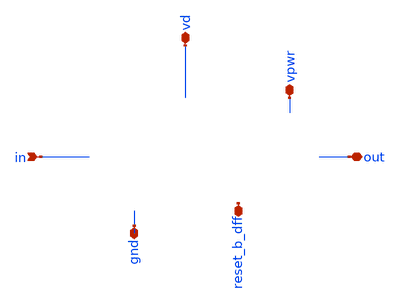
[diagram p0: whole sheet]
** sch_path: sigma-delta_modulator/xschem/sigma-delta-pex.sch
* Copyright 2020 Stefan Frederik Schippers
* Licensed under the Apache License, Version 2.0 (the "License");
* you may not use this file except in compliance with the License.
* You may obtain a copy of the License at
* https://www.apache.org/licenses/LICENSE-2.0
* Unless required by applicable law or agreed to in writing, software
* distributed under the License is distributed on an "AS IS" BASIS,
* WITHOUT WARRANTIES OR CONDITIONS OF ANY KIND, either express or implied.
* See the License for the specific language governing permissions and
* limitations under the License.
**.subckt sigma-delta-pex in gnd out reset_b_dff vpwr vd
*.ipin in
*.iopin gnd
*.iopin out
*.iopin reset_b_dff
*.iopin vpwr
*.iopin vd
**** begin user architecture code



* NGSPICE file created from sigma-delta.ext - technology: sky130A

*.subckt sigma-delta in gnd reset_b_dff vd clk vpwr out
X0 a_n2266_4800# a_n2100_3468# gnd.t0 sky130_fd_pr__res_xhigh_po_0p35 l=4.5
X1 a_n1124_4800# a_n958_3468# gnd.t40 sky130_fd_pr__res_xhigh_po_0p35 l=4.5
X2 vpwr.t5 a_n1599_1969# a_n1612_2361# vpwr.t4 sky130_fd_pr__pfet_01v8_hvt ad=0.0819 pd=0.81
+ as=0.0567 ps=0.69 w=0.42 l=0.15
X3 a_n1599_1969# a_n1774_1995# a_n1420_1995# gnd.t39 sky130_fd_pr__nfet_01v8 ad=0.109 pd=1.36
+ as=0.064 ps=0.725 w=0.42 l=0.15
X4 a_n2231_2361# reset_b_dff.t0 vpwr.t19 vpwr.t18 sky130_fd_pr__pfet_01v8_hvt ad=0.109 pd=1.36
+ as=0.0703 ps=0.755 w=0.42 l=0.15
X5 a_n1599_1969# reset_b_dff.t1 vpwr.t7 vpwr.t6 sky130_fd_pr__pfet_01v8_hvt ad=0.0567 pd=0.69
+ as=0.0819 ps=0.81 w=0.42 l=0.15
X6 x1.Q a_n1599_1969# vpwr.t3 vpwr.t2 sky130_fd_pr__pfet_01v8_hvt ad=0.28 pd=2.56 as=0.213 ps=1.67
+ w=1 l=0.15
X7 out.t0 a_n1035_1995# gnd.t23 gnd.t22 sky130_fd_pr__nfet_01v8 ad=0.169 pd=1.82 as=0.1 ps=0.985
+ w=0.65 l=0.15
X8 a_n2243_1995# a_n2689_1995# a_n2339_1995# gnd.t21 sky130_fd_pr__nfet_01v8 ad=0.14 pd=1.1
+ as=0.0594 ps=0.69 w=0.36 l=0.15
X9 a_n1665_1995# a_n2855_1995# a_n1774_1995# gnd.t19 sky130_fd_pr__nfet_01v8 ad=0.0669 pd=0.75
+ as=0.0711 ps=0.755 w=0.36 l=0.15
X10 gnd.t26 a_n1768_3468# x1.D gnd.t25 sky130_fd_pr__nfet_01v8 ad=0.29 pd=2.58 as=0.29 ps=2.58 w=1
+ l=0.15
X11 a_n792_4800# a_n626_3468# gnd.t38 sky130_fd_pr__res_xhigh_po_0p35 l=4.5
X12 a_n2231_2361# a_n2855_1995# a_n2339_1995# vpwr.t13 sky130_fd_pr__pfet_01v8_hvt ad=0.116 pd=0.97
+ as=0.0724 ps=0.765 w=0.42 l=0.15
X13 a_n2689_1995# a_n2855_1995# gnd.t18 gnd.t17 sky130_fd_pr__nfet_01v8 ad=0.109 pd=1.36 as=0.0567
+ ps=0.69 w=0.42 l=0.15
X14 a_n1934_4800# a_n2100_3468# gnd.t29 sky130_fd_pr__res_xhigh_po_0p35 l=4.5
X15 gnd.t12 reset_b_dff.t2 a_n2077_1995# gnd.t11 sky130_fd_pr__nfet_01v8 ad=0.135 pd=1.15 as=0.0441
+ ps=0.63 w=0.42 l=0.15
X16 a_n2598_4800# a_n2764_3468# gnd.t44 sky130_fd_pr__res_xhigh_po_0p35 l=4.5
X17 gnd.t8 a_n1599_1969# a_n1665_1995# gnd.t7 sky130_fd_pr__nfet_01v8 ad=0.125 pd=1.01 as=0.0669
+ ps=0.75 w=0.42 l=0.15
X18 vd.t1 a_n1768_3468# x1.D vd.t0 sky130_fd_pr__pfet_01v8 ad=0.87 pd=6.58 as=0.87 ps=6.58 w=3
+ l=0.15
X19 a_n1456_4800# a_n1768_3468# gnd.t1 sky130_fd_pr__res_xhigh_po_0p35 l=4.5
X20 vpwr.t1 a_n1599_1969# a_n1035_1995# vpwr.t0 sky130_fd_pr__pfet_01v8_hvt ad=0.154 pd=1.34
+ as=0.166 ps=1.8 w=0.64 l=0.15
X21 a_n1774_1995# a_n2855_1995# a_n2121_2237# vpwr.t12 sky130_fd_pr__pfet_01v8_hvt ad=0.0588 pd=0.7
+ as=0.129 ps=1.18 w=0.42 l=0.15
X22 a_n2077_1995# a_n2121_2237# a_n2243_1995# gnd.t36 sky130_fd_pr__nfet_01v8 ad=0.0441 pd=0.63
+ as=0.14 ps=1.1 w=0.42 l=0.15
X23 a_n2266_4800# a_n2432_3468# gnd.t37 sky130_fd_pr__res_xhigh_po_0p35 l=4.5
X24 a_n1124_4800# a_n1290_3468# gnd.t33 sky130_fd_pr__res_xhigh_po_0p35 l=4.5
X25 a_n2121_2237# a_n2339_1995# vpwr.t9 vpwr.t8 sky130_fd_pr__pfet_01v8_hvt ad=0.129 pd=1.18
+ as=0.218 ps=2.2 w=0.84 l=0.15
X26 a_n460_4800# x1.Q gnd.t13 sky130_fd_pr__res_xhigh_po_0p35 l=4.5
X27 vpwr.t21 clk.t0 a_n2855_1995# vpwr.t20 sky130_fd_pr__pfet_01v8_hvt ad=0.0864 pd=0.91 as=0.166
+ ps=1.8 w=0.64 l=0.15
X28 out.t1 a_n1035_1995# vpwr.t17 vpwr.t16 sky130_fd_pr__pfet_01v8_hvt ad=0.26 pd=2.52 as=0.154
+ ps=1.34 w=1 l=0.15
X29 gnd.t6 a_n1599_1969# a_n1035_1995# gnd.t5 sky130_fd_pr__nfet_01v8 ad=0.1 pd=0.985 as=0.109
+ ps=1.36 w=0.42 l=0.15
X30 vpwr.t23 a_n2121_2237# a_n2231_2361# vpwr.t22 sky130_fd_pr__pfet_01v8_hvt ad=0.0703 pd=0.755
+ as=0.116 ps=0.97 w=0.42 l=0.15
X31 a_n2121_2237# a_n2339_1995# gnd.t15 gnd.t14 sky130_fd_pr__nfet_01v8 ad=0.0999 pd=0.985 as=0.135
+ ps=1.15 w=0.64 l=0.15
X32 a_n1774_1995# a_n2689_1995# a_n2121_2237# gnd.t20 sky130_fd_pr__nfet_01v8 ad=0.0711 pd=0.755
+ as=0.0999 ps=0.985 w=0.36 l=0.15
X33 a_n1612_2361# a_n2689_1995# a_n1774_1995# vpwr.t15 sky130_fd_pr__pfet_01v8_hvt ad=0.0567 pd=0.69
+ as=0.0588 ps=0.7 w=0.42 l=0.15
X34 a_n2339_1995# a_n2855_1995# a_n2434_1995# gnd.t16 sky130_fd_pr__nfet_01v8 ad=0.0594 pd=0.69
+ as=0.066 ps=0.745 w=0.36 l=0.15
X35 a_n2434_1995# x1.D gnd.t42 gnd.t41 sky130_fd_pr__nfet_01v8 ad=0.066 pd=0.745 as=0.221 ps=1.89
+ w=0.42 l=0.15
X36 a_n460_4800# a_n626_3468# gnd.t2 sky130_fd_pr__res_xhigh_po_0p35 l=4.5
X37 a_n2434_1995# x1.D vpwr.t27 vpwr.t26 sky130_fd_pr__pfet_01v8_hvt ad=0.0651 pd=0.73 as=0.109
+ ps=1.36 w=0.42 l=0.15
X38 vpwr.t25 a_n1774_1995# a_n1599_1969# vpwr.t24 sky130_fd_pr__pfet_01v8_hvt ad=0.213 pd=1.67
+ as=0.0567 ps=0.69 w=0.42 l=0.15
X39 a_n2930_4800# a_n2764_3468# gnd.t10 sky130_fd_pr__res_xhigh_po_0p35 l=4.5
X40 gnd.t28 clk.t1 a_n2855_1995# gnd.t27 sky130_fd_pr__nfet_01v8 ad=0.0567 pd=0.69 as=0.109 ps=1.36
+ w=0.42 l=0.15
X41 a_n1768_3468# gnd.t24 sky130_fd_pr__cap_mim_m3_1 l=27.2 w=27.2
X42 a_n1420_1995# reset_b_dff.t3 gnd.t32 gnd.t31 sky130_fd_pr__nfet_01v8 ad=0.064 pd=0.725 as=0.125
+ ps=1.01 w=0.42 l=0.15
X43 a_n1934_4800# a_n1768_3468# gnd.t34 sky130_fd_pr__res_xhigh_po_0p35 l=4.5
X44 a_n792_4800# a_n958_3468# gnd.t35 sky130_fd_pr__res_xhigh_po_0p35 l=4.5
X45 a_n2598_4800# a_n2432_3468# gnd.t9 sky130_fd_pr__res_xhigh_po_0p35 l=4.5
X46 a_n2339_1995# a_n2689_1995# a_n2434_1995# vpwr.t14 sky130_fd_pr__pfet_01v8_hvt ad=0.0724
+ pd=0.765 as=0.0651 ps=0.73 w=0.42 l=0.15
X47 a_n2930_4800# in.t0 gnd.t43 sky130_fd_pr__res_xhigh_po_0p35 l=4.5
X48 a_n1456_4800# a_n1290_3468# gnd.t30 sky130_fd_pr__res_xhigh_po_0p35 l=4.5
X49 a_n2689_1995# a_n2855_1995# vpwr.t11 vpwr.t10 sky130_fd_pr__pfet_01v8_hvt ad=0.166 pd=1.8
+ as=0.0864 ps=0.91 w=0.64 l=0.15
X50 x1.Q a_n1599_1969# gnd.t4 gnd.t3 sky130_fd_pr__nfet_01v8 ad=0.169 pd=1.82 as=0.169 ps=1.82
+ w=0.65 l=0.15
R0 gnd.n65 gnd.t13 3132.98
R1 gnd.t22 gnd.n73 441.774
R2 gnd.t17 gnd.t41 411.14
R3 gnd.t13 gnd.t2 324.911
R4 gnd.t3 gnd.t5 303.115
R5 gnd.t39 gnd.t3 303.115
R6 gnd.n73 gnd.n72 301.113
R7 gnd.t1 gnd.n2 283.973
R8 gnd.t2 gnd.t38 275.286
R9 gnd.t21 gnd.t36 267.644
R10 gnd.t38 gnd.t35 259.007
R11 gnd.t35 gnd.t40 259.007
R12 gnd.t40 gnd.t33 259.007
R13 gnd.t33 gnd.t30 259.007
R14 gnd.t30 gnd.t1 259.007
R15 gnd.t34 gnd.t29 259.007
R16 gnd.t29 gnd.t0 259.007
R17 gnd.t0 gnd.t37 259.007
R18 gnd.t37 gnd.t9 259.007
R19 gnd.t9 gnd.t44 259.007
R20 gnd.t44 gnd.t10 259.007
R21 gnd.t10 gnd.t43 259.007
R22 gnd.t7 gnd.t31 240.236
R23 gnd.n48 gnd.t42 215.036
R24 gnd.t11 gnd.t14 212.826
R25 gnd.n2 gnd.t34 202.838
R26 gnd.t20 gnd.t19 175.743
R27 gnd.t14 gnd.t20 159.619
R28 gnd.t5 gnd.t22 156.394
R29 gnd.t19 gnd.t7 154.782
R30 gnd.t16 gnd.t21 154.782
R31 gnd.n23 gnd.t4 154.317
R32 gnd.t41 gnd.t16 153.171
R33 gnd.n70 gnd.n1 149.835
R34 gnd.n70 gnd.n69 149.835
R35 gnd.t31 gnd.t39 146.72
R36 gnd.t27 gnd.t17 135.435
R37 gnd.n24 gnd.n22 128.757
R38 gnd.n30 gnd.n29 116.754
R39 gnd.t36 gnd.t11 116.087
R40 gnd.n17 gnd.n16 107.24
R41 gnd.n52 gnd.n12 107.24
R42 gnd gnd.t27 104.8
R43 gnd.n29 gnd.t32 100.001
R44 gnd.n69 gnd.n67 98.6358
R45 gnd.n16 gnd.t12 72.8576
R46 gnd.n29 gnd.t8 70.0005
R47 gnd.n16 gnd.t15 60.5809
R48 gnd.n22 gnd.t6 57.1434
R49 gnd.n12 gnd.t18 38.5719
R50 gnd.n12 gnd.t28 38.5719
R51 gnd.n27 gnd.n21 34.6358
R52 gnd.n28 gnd.n27 34.6358
R53 gnd.n31 gnd.n19 34.6358
R54 gnd.n35 gnd.n19 34.6358
R55 gnd.n36 gnd.n35 34.6358
R56 gnd.n37 gnd.n36 34.6358
R57 gnd.n41 gnd.n40 34.6358
R58 gnd.n42 gnd.n41 34.6358
R59 gnd.n42 gnd.n14 34.6358
R60 gnd.n46 gnd.n14 34.6358
R61 gnd.n47 gnd.n46 34.6358
R62 gnd.n48 gnd.n11 29.7417
R63 gnd.n23 gnd.n21 27.8593
R64 gnd.n22 gnd.t23 25.4291
R65 gnd.n53 gnd.n52 24.4919
R66 gnd.n52 gnd.n11 22.9652
R67 gnd.n30 gnd.n28 17.6946
R68 gnd.n6 gnd.t26 17.405
R69 gnd.n48 gnd.n47 14.6829
R70 gnd.n24 gnd.n23 10.9075
R71 gnd.n6 gnd.n5 9.33321
R72 gnd.n40 gnd.n17 7.90638
R73 gnd.n52 gnd.n51 4.6505
R74 gnd.n25 gnd.n21 4.6505
R75 gnd.n27 gnd.n26 4.6505
R76 gnd.n28 gnd.n20 4.6505
R77 gnd.n32 gnd.n31 4.6505
R78 gnd.n33 gnd.n19 4.6505
R79 gnd.n35 gnd.n34 4.6505
R80 gnd.n36 gnd.n18 4.6505
R81 gnd.n38 gnd.n37 4.6505
R82 gnd.n40 gnd.n39 4.6505
R83 gnd.n41 gnd.n15 4.6505
R84 gnd.n43 gnd.n42 4.6505
R85 gnd.n44 gnd.n14 4.6505
R86 gnd.n46 gnd.n45 4.6505
R87 gnd.n47 gnd.n13 4.6505
R88 gnd.n49 gnd.n48 4.6505
R89 gnd.n50 gnd.n11 4.6505
R90 gnd.n55 gnd.n10 4.5005
R91 gnd.n55 gnd.n54 4.5005
R92 gnd gnd.n56 3.79922
R93 gnd.n58 gnd.n57 2.6505
R94 gnd.n31 gnd.n30 2.63579
R95 gnd.n55 gnd.n9 2.25328
R96 gnd.n37 gnd.n17 1.88285
R97 gnd.n57 gnd.t24 1.47915
R98 gnd.n57 gnd 1.25931
R99 gnd.n67 gnd.n66 0.541165
R100 gnd.n66 gnd.n65 0.541165
R101 gnd.n64 gnd.n63 0.347269
R102 gnd.n65 gnd.n64 0.347269
R103 gnd.n25 gnd.n24 0.144332
R104 gnd.n26 gnd.n25 0.120292
R105 gnd.n26 gnd.n20 0.120292
R106 gnd.n32 gnd.n20 0.120292
R107 gnd.n33 gnd.n32 0.120292
R108 gnd.n34 gnd.n33 0.120292
R109 gnd.n34 gnd.n18 0.120292
R110 gnd.n38 gnd.n18 0.120292
R111 gnd.n39 gnd.n38 0.120292
R112 gnd.n39 gnd.n15 0.120292
R113 gnd.n43 gnd.n15 0.120292
R114 gnd.n44 gnd.n43 0.120292
R115 gnd.n45 gnd.n44 0.120292
R116 gnd.n45 gnd.n13 0.120292
R117 gnd.n49 gnd.n13 0.120292
R118 gnd.n50 gnd.n49 0.120292
R119 gnd.n51 gnd.n50 0.120292
R120 gnd.n1 gnd.n0 0.10956
R121 gnd.n0 gnd.t25 0.10956
R122 gnd.n69 gnd.n68 0.10956
R123 gnd.n62 gnd.n4 0.084913
R124 gnd.n4 gnd.n3 0.0845034
R125 gnd.n51 gnd.n10 0.0734167
R126 gnd.n71 gnd.n70 0.0425017
R127 gnd.n72 gnd.n71 0.0425017
R128 gnd.n54 gnd 0.0330521
R129 gnd.n10 gnd.n8 0.0265417
R130 gnd gnd.n53 0.0226354
R131 gnd.n9 gnd.n8 0.0114272
R132 gnd.n53 gnd.n9 0.0113582
R133 gnd.n56 gnd.n55 0.0110001
R134 gnd.n59 gnd.n6 0.00867757
R135 gnd.n59 gnd.n58 0.00634112
R136 gnd.n54 gnd 0.00570833
R137 gnd.n62 gnd.n61 0.00440917
R138 gnd.n61 gnd.n60 0.00391284
R139 gnd.n60 gnd.n59 0.00391159
R140 gnd.n56 gnd.n8 0.00100955
R141 gnd.n65 gnd.n62 0.00100353
R142 gnd.n58 gnd.n7 0.00051897
R143 vpwr.t10 vpwr.t26 790.188
R144 vpwr.t2 vpwr.t0 648.131
R145 vpwr.t18 vpwr.t8 583.023
R146 vpwr.n45 vpwr 548.548
R147 vpwr.n26 vpwr.t9 514.011
R148 vpwr.t24 vpwr.t2 485.358
R149 vpwr.t13 vpwr.t22 414.33
R150 vpwr.n2 vpwr.t27 375.277
R151 vpwr.t4 vpwr.t6 319.627
R152 vpwr.n20 vpwr.n9 311.957
R153 vpwr.n42 vpwr.n1 311.894
R154 vpwr.n29 vpwr.n28 309.18
R155 vpwr.t8 vpwr.t12 292.991
R156 vpwr.t14 vpwr.t13 292.991
R157 vpwr.n13 vpwr.n10 292.5
R158 vpwr.n15 vpwr.n14 292.5
R159 vpwr.t0 vpwr.t16 287.072
R160 vpwr.t22 vpwr.t18 287.072
R161 vpwr.t26 vpwr.t14 272.274
R162 vpwr.t12 vpwr.t15 254.518
R163 vpwr.t6 vpwr.t24 248.599
R164 vpwr.t15 vpwr.t4 248.599
R165 vpwr.t20 vpwr.t10 244.306
R166 vpwr vpwr.t20 186.556
R167 vpwr.n14 vpwr.n13 182.929
R168 vpwr.n12 vpwr.n11 148.689
R169 vpwr.n9 vpwr.t5 119.608
R170 vpwr.n28 vpwr.t23 93.81
R171 vpwr.n13 vpwr.t25 68.0124
R172 vpwr.n28 vpwr.t19 63.3219
R173 vpwr.n9 vpwr.t7 63.3219
R174 vpwr.n11 vpwr.t1 61.9158
R175 vpwr.n1 vpwr.t11 41.5552
R176 vpwr.n1 vpwr.t21 41.5552
R177 vpwr.n41 vpwr.n40 34.6358
R178 vpwr.n34 vpwr.n4 34.6358
R179 vpwr.n35 vpwr.n34 34.6358
R180 vpwr.n36 vpwr.n35 34.6358
R181 vpwr.n30 vpwr.n27 34.6358
R182 vpwr.n21 vpwr.n7 34.6358
R183 vpwr.n25 vpwr.n7 34.6358
R184 vpwr.n36 vpwr.n2 32.377
R185 vpwr.n26 vpwr.n25 32.0005
R186 vpwr.n11 vpwr.t17 30.239
R187 vpwr.n20 vpwr.n19 30.1181
R188 vpwr.n14 vpwr.t3 29.316
R189 vpwr.n42 vpwr.n41 22.9652
R190 vpwr.n21 vpwr.n20 20.3299
R191 vpwr.n40 vpwr.n2 18.0711
R192 vpwr.n15 vpwr.n12 13.9946
R193 vpwr.n19 vpwr.n10 12.8758
R194 vpwr.n27 vpwr.n26 9.41227
R195 vpwr.n29 vpwr.n4 6.02403
R196 vpwr.n16 vpwr.n15 5.00414
R197 vpwr.n20 vpwr.n8 4.6505
R198 vpwr.n26 vpwr.n6 4.6505
R199 vpwr.n38 vpwr.n2 4.6505
R200 vpwr.n17 vpwr.n16 4.6505
R201 vpwr.n19 vpwr.n18 4.6505
R202 vpwr.n22 vpwr.n21 4.6505
R203 vpwr.n23 vpwr.n7 4.6505
R204 vpwr.n25 vpwr.n24 4.6505
R205 vpwr.n27 vpwr.n5 4.6505
R206 vpwr.n31 vpwr.n30 4.6505
R207 vpwr.n32 vpwr.n4 4.6505
R208 vpwr.n34 vpwr.n33 4.6505
R209 vpwr.n35 vpwr.n3 4.6505
R210 vpwr.n37 vpwr.n36 4.6505
R211 vpwr.n40 vpwr.n39 4.6505
R212 vpwr.n41 vpwr.n0 4.6505
R213 vpwr.n16 vpwr.n10 4.07323
R214 vpwr.n43 vpwr.n42 3.93272
R215 vpwr.n30 vpwr.n29 3.76521
R216 vpwr vpwr.n51 0.223
R217 vpwr.n17 vpwr.n12 0.144332
R218 vpwr.n43 vpwr.n0 0.138831
R219 vpwr.n18 vpwr.n17 0.120292
R220 vpwr.n18 vpwr.n8 0.120292
R221 vpwr.n22 vpwr.n8 0.120292
R222 vpwr.n23 vpwr.n22 0.120292
R223 vpwr.n24 vpwr.n23 0.120292
R224 vpwr.n24 vpwr.n6 0.120292
R225 vpwr.n6 vpwr.n5 0.120292
R226 vpwr.n31 vpwr.n5 0.120292
R227 vpwr.n32 vpwr.n31 0.120292
R228 vpwr.n33 vpwr.n32 0.120292
R229 vpwr.n33 vpwr.n3 0.120292
R230 vpwr.n37 vpwr.n3 0.120292
R231 vpwr.n38 vpwr.n37 0.120292
R232 vpwr.n39 vpwr.n38 0.120292
R233 vpwr.n39 vpwr.n0 0.120292
R234 vpwr.n44 vpwr.n43 0.107496
R235 vpwr.n47 vpwr 0.088
R236 vpwr.n51 vpwr.n50 0.0197304
R237 vpwr.n44 vpwr 0.0174271
R238 vpwr vpwr.n44 0.01675
R239 vpwr.n48 vpwr.n47 0.013
R240 vpwr.n50 vpwr.n49 0.00412567
R241 vpwr.n49 vpwr.n48 0.003625
R242 vpwr.n50 vpwr.n45 0.0015496
R243 vpwr.n49 vpwr.n46 0.000543305
R244 reset_b_dff.n14 reset_b_dff.t0 413.313
R245 reset_b_dff.n7 reset_b_dff.t1 344.005
R246 reset_b_dff.n6 reset_b_dff.t3 187.321
R247 reset_b_dff.n7 reset_b_dff.n5 152
R248 reset_b_dff.n14 reset_b_dff.t2 126.127
R249 reset_b_dff.n6 reset_b_dff.n1 73.2067
R250 reset_b_dff reset_b_dff.n4 14.0185
R251 reset_b_dff.n11 reset_b_dff.n10 9.3005
R252 reset_b_dff.n8 reset_b_dff.n2 9.3005
R253 reset_b_dff.n8 reset_b_dff.n7 9.3005
R254 reset_b_dff.n7 reset_b_dff.n6 9.15991
R255 reset_b_dff.n15 reset_b_dff.n14 7.02742
R256 reset_b_dff.n4 reset_b_dff 4.7293
R257 reset_b_dff.n9 reset_b_dff.n0 4.6505
R258 reset_b_dff.n18 reset_b_dff.n17 4.6505
R259 reset_b_dff.n4 reset_b_dff 4.53383
R260 reset_b_dff.n5 reset_b_dff 3.11401
R261 reset_b_dff.n17 reset_b_dff.n15 3.0725
R262 reset_b_dff.n24 reset_b_dff 2.98033
R263 reset_b_dff.n12 reset_b_dff 2.36657
R264 reset_b_dff.n5 reset_b_dff.n1 1.55726
R265 reset_b_dff.n10 reset_b_dff.n9 1.55726
R266 reset_b_dff.n8 reset_b_dff.n1 1.38428
R267 reset_b_dff.n9 reset_b_dff.n8 1.38428
R268 reset_b_dff.n10 reset_b_dff 1.38428
R269 reset_b_dff.n17 reset_b_dff.n16 1.2805
R270 reset_b_dff.n12 reset_b_dff 0.580857
R271 reset_b_dff.n3 reset_b_dff 0.196446
R272 reset_b_dff.n20 reset_b_dff 0.171696
R273 reset_b_dff.n20 reset_b_dff.n19 0.0901739
R274 reset_b_dff.n21 reset_b_dff.n20 0.0500874
R275 reset_b_dff.n13 reset_b_dff.n12 0.0466957
R276 reset_b_dff.n26 reset_b_dff.n25 0.0435328
R277 reset_b_dff.n18 reset_b_dff.n13 0.0331087
R278 reset_b_dff.n3 reset_b_dff.n2 0.02675
R279 reset_b_dff reset_b_dff.n11 0.0255
R280 reset_b_dff.n22 reset_b_dff.n21 0.0213989
R281 reset_b_dff.n24 reset_b_dff.n23 0.018111
R282 reset_b_dff.n19 reset_b_dff.n18 0.014087
R283 reset_b_dff.n25 reset_b_dff.n22 0.0127951
R284 reset_b_dff.n11 reset_b_dff.n0 0.01175
R285 reset_b_dff.n2 reset_b_dff.n0 0.0105
R286 reset_b_dff reset_b_dff.n3 0.00725676
R287 reset_b_dff reset_b_dff.n26 0.00459836
R288 reset_b_dff.n25 reset_b_dff.n24 0.0016109
R289 out.n0 out.t1 250.94
R290 out out.t0 144.601
R291 out.n0 out 4.7225
R292 out out.n0 3.35288
R293 vd.n10 vd.n7 135.465
R294 vd.n13 vd.n12 101.647
R295 vd.n26 vd.t1 9.52337
R296 vd vd.n35 2.4755
R297 vd.n14 vd.n13 0.130052
R298 vd.n15 vd.n14 0.130052
R299 vd.n5 vd.n4 0.107375
R300 vd.n15 vd.n5 0.107375
R301 vd.n31 vd.n29 0.0456031
R302 vd.n25 vd.n23 0.0456031
R303 vd.n23 vd.n21 0.0456031
R304 vd.n34 vd.n33 0.0391598
R305 vd.n33 vd.n31 0.0391598
R306 vd.n12 vd.n11 0.0349892
R307 vd.n11 vd.t0 0.0349892
R308 vd.n9 vd.n8 0.0349892
R309 vd.n10 vd.n9 0.0333079
R310 vd.n26 vd.n25 0.0217629
R311 vd.n29 vd.n27 0.0198299
R312 vd.n16 vd.n3 0.0125538
R313 vd.n3 vd.n2 0.0120596
R314 vd.n7 vd.n6 0.00627981
R315 vd.n27 vd.n26 0.00501031
R316 vd.t0 vd.n10 0.00318081
R317 vd.n17 vd.n16 0.0018171
R318 vd.n18 vd.n17 0.00131751
R319 vd.n27 vd.n18 0.00131744
R320 vd.n33 vd.n32 0.00119114
R321 vd.n34 vd.n0 0.00101609
R322 vd.n16 vd.n15 0.00100038
R323 vd.n21 vd.n20 0.00100009
R324 vd.n29 vd.n28 0.000659706
R325 vd.n23 vd.n22 0.000659706
R326 vd.n31 vd.n1 0.000543686
R327 vd.n25 vd.n19 0.000543686
R328 vd.n35 vd.n34 0.000507883
R329 vd.n25 vd.n24 0.000507883
R330 vd.n31 vd.n30 0.000507883
R331 clk.n3 clk.t0 294.557
R332 clk.n3 clk.t1 211.01
R333 clk.n4 clk.n3 8.28655
R334 clk.n2 clk 7.73487
R335 clk.n4 clk.n2 1.82961
R336 clk clk.n5 0.981259
R337 clk.n5 clk.n4 0.848973
R338 clk.n0 clk 0.385917
R339 clk.n1 clk.n0 0.03175
R340 clk.n2 clk.n1 0.00111796
R341 in in.t0 9.56433
C0 a_n792_4800# a_n626_3468# 0.00473f
C1 a_n2434_1995# a_n2855_1995# 0.0931f
C2 a_n1665_1995# x1.Q 1.47e-19
C3 a_n1774_1995# vd 3.52e-19
C4 out a_n1035_1995# 0.0691f
C5 clk a_n1665_1995# 1.1e-20
C6 x1.Q a_n1599_1969# 0.142f
C7 vpwr a_n1599_1969# 0.408f
C8 a_n1290_3468# vd 0.00171f
C9 a_n1035_1995# x1.D 0.00209f
C10 a_n2689_1995# a_n2231_2361# 0.0346f
C11 a_n1665_1995# reset_b_dff 7.93e-19
C12 a_n2121_2237# a_n1612_2361# 2.6e-19
C13 a_n2121_2237# a_n2689_1995# 0.186f
C14 clk a_n1599_1969# 2.68e-20
C15 a_n2432_3468# a_n2100_3468# 0.302f
C16 a_n1934_4800# a_n2266_4800# 0.296f
C17 a_n1768_3468# a_n2764_3468# 2.04e-19
C18 a_n2434_1995# x1.D 0.164f
C19 a_n1768_3468# a_n2855_1995# 1.78e-19
C20 a_n1774_1995# a_n1665_1995# 0.00742f
C21 reset_b_dff a_n1599_1969# 0.28f
C22 a_n958_3468# a_n1290_3468# 0.312f
C23 a_n1768_3468# in 6.8e-20
C24 a_n1774_1995# a_n1599_1969# 0.251f
C25 a_n792_4800# x1.Q 0.0032f
C26 a_n1124_4800# a_n1290_3468# 0.00536f
C27 a_n2689_1995# a_n2432_3468# 1.82e-19
C28 vd a_n1456_4800# 5.85e-19
C29 a_n2689_1995# a_n1612_2361# 1.46e-19
C30 a_n1290_3468# a_n1599_1969# 4.27e-19
C31 a_n1934_4800# a_n2100_3468# 0.00434f
C32 a_n1768_3468# out 0.16f
C33 a_n2121_2237# a_n1665_1995# 4.2e-19
C34 a_n1768_3468# x1.D 0.339f
C35 a_n2689_1995# vd 1.08e-19
C36 a_n1934_4800# a_n1456_4800# 0.144f
C37 vd a_n460_4800# 0.133f
C38 out a_n626_3468# 7.61e-19
C39 a_n1124_4800# a_n1456_4800# 0.3f
C40 x1.D a_n626_3468# 2.69e-19
C41 a_n1768_3468# a_n1035_1995# 0.00366f
C42 a_n2689_1995# a_n1665_1995# 2.36e-20
C43 a_n2764_3468# vpwr 0.0038f
C44 a_n958_3468# vd 0.00352f
C45 a_n1934_4800# vd 6.34e-20
C46 a_n2855_1995# a_n2339_1995# 0.115f
C47 a_n2243_1995# a_n2855_1995# 0.00134f
C48 a_n2077_1995# a_n2339_1995# 0.00171f
C49 x1.Q a_n2855_1995# 9.54e-19
C50 a_n2077_1995# x1.Q 9.75e-20
C51 vpwr a_n2855_1995# 0.441f
C52 a_n2689_1995# a_n1599_1969# 0.0426f
C53 a_n2266_4800# a_n2598_4800# 0.303f
C54 a_n1124_4800# vd 0.00116f
C55 clk a_n2855_1995# 0.273f
C56 vpwr in 7.19e-19
C57 a_n1420_1995# x1.D 4.54e-20
C58 clk a_n2077_1995# 1.82e-20
C59 vd a_n1599_1969# 0.00172f
C60 reset_b_dff a_n2855_1995# 0.312f
C61 a_n2077_1995# reset_b_dff 0.00407f
C62 out a_n2339_1995# 7.05e-19
C63 a_n958_3468# a_n1124_4800# 0.00509f
C64 out x1.Q 0.668f
C65 out vpwr 0.577f
C66 a_n2339_1995# x1.D 0.00353f
C67 a_n2243_1995# x1.D 8.22e-19
C68 a_n1774_1995# a_n2855_1995# 0.102f
C69 x1.Q x1.D 0.0675f
C70 vpwr x1.D 0.238f
C71 a_n958_3468# a_n1599_1969# 1.28e-20
C72 clk out 4.76e-19
C73 clk x1.D 0.0102f
C74 a_n792_4800# vd 0.00299f
C75 out reset_b_dff 0.00564f
C76 a_n792_4800# a_n460_4800# 0.299f
C77 a_n1290_3468# in 9.87e-22
C78 reset_b_dff x1.D 0.223f
C79 a_n2231_2361# a_n2855_1995# 9.73e-19
C80 x1.Q a_n1035_1995# 0.226f
C81 a_n1768_3468# a_n626_3468# 0.00957f
C82 vpwr a_n1035_1995# 0.198f
C83 a_n1774_1995# out 6.85e-19
C84 a_n2121_2237# a_n2855_1995# 0.0701f
C85 a_n2121_2237# a_n2077_1995# 3.69e-19
C86 a_n1774_1995# x1.D 9.45e-19
C87 a_n2598_4800# a_n2432_3468# 0.00482f
C88 a_n792_4800# a_n958_3468# 0.00482f
C89 a_n2434_1995# a_n2339_1995# 0.0498f
C90 a_n2434_1995# a_n2243_1995# 4.61e-19
C91 a_n2434_1995# x1.Q 7.58e-20
C92 a_n2100_3468# in 1.53e-20
C93 a_n2434_1995# vpwr 0.0827f
C94 a_n2930_4800# a_n2598_4800# 0.296f
C95 reset_b_dff a_n1035_1995# 0.00144f
C96 a_n792_4800# a_n1124_4800# 0.307f
C97 clk a_n2434_1995# 3.09e-19
C98 a_n2764_3468# a_n2432_3468# 0.296f
C99 a_n2121_2237# out 3.73e-19
C100 a_n1774_1995# a_n1035_1995# 7.05e-19
C101 a_n2231_2361# x1.D 5.56e-20
C102 a_n2855_1995# a_n2432_3468# 1.92e-19
C103 out a_n2100_3468# 0.0148f
C104 a_n2434_1995# reset_b_dff 0.00224f
C105 a_n2689_1995# a_n2855_1995# 0.906f
C106 a_n2121_2237# x1.D 6.24e-19
C107 a_n2764_3468# a_n2930_4800# 0.00458f
C108 a_n2432_3468# in 4.07e-20
C109 vd a_n2855_1995# 1.72e-20
C110 a_n1768_3468# a_n2339_1995# 2.02e-20
C111 a_n1768_3468# x1.Q 0.414f
C112 a_n1768_3468# vpwr 0.0129f
C113 a_n2930_4800# in 0.0056f
C114 out a_n2432_3468# 0.0146f
C115 a_n2689_1995# out 0.0011f
C116 x1.D a_n2432_3468# 2.56e-20
C117 x1.D a_n1612_2361# 2.11e-20
C118 a_n2689_1995# x1.D 0.229f
C119 a_n1768_3468# reset_b_dff 2.83e-19
C120 x1.Q a_n626_3468# 0.414f
C121 a_n1665_1995# a_n2855_1995# 2.56e-19
C122 out vd 0.0503f
C123 vd x1.D 0.908f
C124 a_n1768_3468# a_n1774_1995# 0.0011f
C125 a_n1599_1969# a_n2855_1995# 0.0436f
C126 a_n1768_3468# a_n1290_3468# 0.357f
C127 a_n2689_1995# a_n1035_1995# 2.01e-19
C128 a_n1420_1995# x1.Q 6.05e-19
C129 vd a_n1035_1995# 0.00317f
C130 a_n1665_1995# x1.D 2.42e-20
C131 a_n2689_1995# a_n2434_1995# 0.0642f
C132 clk a_n1420_1995# 6.32e-21
C133 a_n2121_2237# a_n1768_3468# 7.49e-21
C134 a_n1768_3468# a_n2100_3468# 0.298f
C135 out a_n1599_1969# 0.00735f
C136 a_n2243_1995# a_n2339_1995# 0.0138f
C137 x1.Q a_n2339_1995# 8.11e-19
C138 a_n2243_1995# x1.Q 1.45e-19
C139 a_n1599_1969# x1.D 0.004f
C140 vpwr a_n2339_1995# 0.197f
C141 a_n1420_1995# reset_b_dff 0.00312f
C142 x1.Q vpwr 0.175f
C143 a_n958_3468# a_n1035_1995# 1.4e-19
C144 clk a_n2339_1995# 3.26e-19
C145 clk a_n2243_1995# 5.33e-20
C146 a_n1768_3468# a_n1456_4800# 0.00837f
C147 clk vpwr 0.19f
C148 reset_b_dff a_n2339_1995# 0.165f
C149 a_n2243_1995# reset_b_dff 0.00292f
C150 reset_b_dff x1.Q 0.0107f
C151 a_n1768_3468# a_n2432_3468# 4.38e-19
C152 reset_b_dff vpwr 0.205f
C153 a_n1768_3468# a_n1612_2361# 5.54e-20
C154 a_n2689_1995# a_n1768_3468# 4.13e-19
C155 a_n2764_3468# a_n2598_4800# 0.00434f
C156 a_n1035_1995# a_n1599_1969# 0.107f
C157 a_n1774_1995# a_n2339_1995# 7.99e-20
C158 clk reset_b_dff 0.0302f
C159 a_n1774_1995# x1.Q 0.00593f
C160 a_n1774_1995# vpwr 0.284f
C161 a_n1768_3468# vd 0.743f
C162 a_n1768_3468# a_n460_4800# 0.0109f
C163 x1.Q a_n1290_3468# 1.87e-20
C164 clk a_n1774_1995# 6.46e-20
C165 vpwr a_n1290_3468# 0.00384f
C166 a_n2764_3468# a_n2855_1995# 1.47e-19
C167 a_n1774_1995# reset_b_dff 0.239f
C168 a_n958_3468# a_n1768_3468# 0.0502f
C169 vd a_n626_3468# 0.0154f
C170 a_n2231_2361# a_n2339_1995# 0.0572f
C171 a_n1768_3468# a_n1934_4800# 0.00466f
C172 a_n460_4800# a_n626_3468# 0.00434f
C173 a_n2231_2361# x1.Q 3.66e-19
C174 a_n2231_2361# vpwr 0.143f
C175 a_n2121_2237# a_n2339_1995# 0.21f
C176 a_n2121_2237# a_n2243_1995# 3.16e-19
C177 a_n2764_3468# in 0.303f
C178 a_n2121_2237# x1.Q 0.00111f
C179 a_n2339_1995# a_n2100_3468# 1.22e-19
C180 a_n1768_3468# a_n1665_1995# 1.36e-20
C181 a_n2121_2237# vpwr 0.205f
C182 x1.Q a_n2100_3468# 1.43e-21
C183 vpwr a_n2100_3468# 0.0038f
C184 a_n1768_3468# a_n1124_4800# 0.00679f
C185 clk a_n2121_2237# 1.78e-19
C186 a_n1768_3468# a_n1599_1969# 0.00381f
C187 a_n958_3468# a_n626_3468# 0.303f
C188 a_n2231_2361# reset_b_dff 0.013f
C189 a_n2764_3468# out 0.0146f
C190 a_n2121_2237# reset_b_dff 0.172f
C191 a_n2764_3468# x1.D 2.07e-19
C192 out a_n2855_1995# 0.00153f
C193 reset_b_dff a_n2100_3468# 1.77e-19
C194 a_n2855_1995# x1.D 0.195f
C195 a_n2077_1995# x1.D 5.41e-20
C196 a_n2689_1995# a_n2339_1995# 0.23f
C197 a_n2689_1995# a_n2243_1995# 2.28e-19
C198 a_n2121_2237# a_n1774_1995# 0.0512f
C199 x1.Q a_n1612_2361# 4.53e-20
C200 vpwr a_n2432_3468# 0.00379f
C201 a_n2689_1995# x1.Q 0.00137f
C202 out in 0.0195f
C203 vpwr a_n1612_2361# 7.36e-19
C204 a_n2689_1995# vpwr 0.57f
C205 a_n2266_4800# a_n2100_3468# 0.00473f
C206 clk a_n2689_1995# 0.00241f
C207 x1.Q vd 0.0964f
C208 x1.Q a_n460_4800# 0.00839f
C209 vpwr vd 0.00696f
C210 a_n792_4800# a_n1768_3468# 0.00627f
C211 reset_b_dff a_n1612_2361# 2.06e-19
C212 a_n2689_1995# reset_b_dff 0.0304f
C213 a_n1035_1995# a_n2855_1995# 4.71e-20
C214 out x1.D 0.294f
C215 a_n2121_2237# a_n2231_2361# 0.0977f
C216 a_n1290_3468# a_n1456_4800# 0.00473f
C217 a_n1420_1995# a_n1599_1969# 0.0074f
C218 a_n2266_4800# a_n2432_3468# 0.00473f
C219 a_n1774_1995# a_n1612_2361# 0.00645f
C220 a_n2689_1995# a_n1774_1995# 0.125f
C221 a_n2121_2237# a_n2100_3468# 7.2e-20
C222 a_n958_3468# x1.Q 5e-20
C223 reset_b_dff vd 2.96e-19
C224 a_n958_3468# vpwr 0.00266f
C225 out gnd 1.01f
C226 reset_b_dff gnd 1.4f
C227 clk gnd 0.346f
C228 in gnd 0.505f
C229 vd gnd 3.47f
C230 vpwr gnd 2.9f
C231 a_n1420_1995# gnd 0.00223f
C232 a_n1665_1995# gnd 9.68e-19
C233 a_n2077_1995# gnd 0.00579f
C234 a_n2243_1995# gnd 0.00863f
C235 a_n2231_2361# gnd 0.00469f
C236 a_n2434_1995# gnd 0.08f
C237 a_n1035_1995# gnd 0.213f
C238 a_n1774_1995# gnd 0.275f
C239 a_n1599_1969# gnd 0.74f
C240 a_n2339_1995# gnd 0.281f
C241 a_n2121_2237# gnd 0.194f
C242 a_n2689_1995# gnd 0.332f
C243 x1.D gnd 2.58f
C244 a_n2855_1995# gnd 0.7f
C245 x1.Q gnd 1.09f
C246 a_n460_4800# gnd 0.559f
C247 a_n626_3468# gnd 0.348f
C248 a_n792_4800# gnd 0.388f
C249 a_n958_3468# gnd 0.356f
C250 a_n1124_4800# gnd 0.392f
C251 a_n1290_3468# gnd 0.357f
C252 a_n1456_4800# gnd 0.447f
C253 a_n1768_3468# gnd 70f
C254 a_n1934_4800# gnd 0.449f
C255 a_n2100_3468# gnd 0.365f
C256 a_n2266_4800# gnd 0.387f
C257 a_n2432_3468# gnd 0.364f
C258 a_n2598_4800# gnd 0.39f
C259 a_n2764_3468# gnd 0.366f
C260 a_n2930_4800# gnd 0.604f
*.ends





.include /foss/pdks/sky130A/libs.ref/sky130_fd_sc_hd/spice/sky130_fd_sc_hd.spice


**** end user architecture code
**.ends
.end
